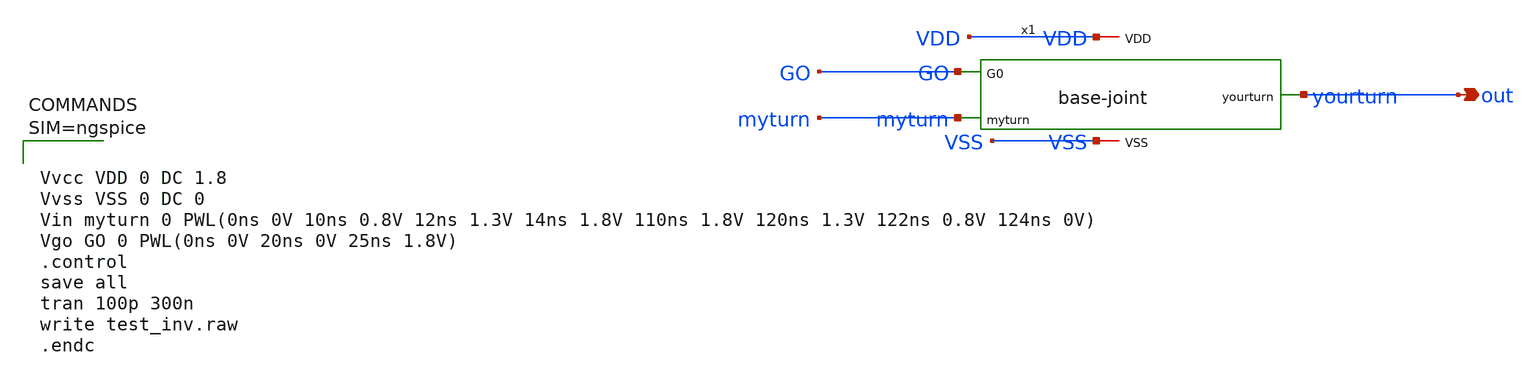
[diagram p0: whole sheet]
** sch_path: xschem/testbench.sch
**.subckt testbench out
*.opin out
x1 VSS VDD GO yourturn myturn base-joint
**** begin user architecture code

** opencircuitdesign pdks install
.lib $::SKYWATER_MODELS/sky130.lib.spice tt
.include $::SKYWATER_STDCELLS/sky130_fd_sc_hd.spice tt




Vvcc VDD 0 DC 1.8
Vvss VSS 0 DC 0
Vin myturn 0 PWL(0ns 0V 10ns 0.8V 12ns 1.3V 14ns 1.8V 110ns 1.8V 120ns 1.3V 122ns 0.8V 124ns 0V)
Vgo GO 0 PWL(0ns 0V 20ns 0V 25ns 1.8V)
.control
save all
tran 100p 300n
write test_inv.raw
.endc



**** end user architecture code
**.ends

* expanding   symbol:  base-joint.sym # of pins=5
** sym_path: xschem/base-joint.sym
** sch_path: xschem/base-joint.sch
.subckt base-joint VSS VDD G0 yourturn myturn
*.ipin G0
*.ipin myturn
*.opin yourturn
*.iopin VDD
*.iopin VSS
Mr net1 myturn VSS VSS VDD VDD yourturn sky130_fd_sc_hd__and2_0
Go net2 yourturn VSS VSS VDD VDD net1 sky130_fd_sc_hd__and2_0
inverter G0 VSS VSS VDD VDD net2 sky130_fd_sc_hd__clkinv_8
.ends

.end
